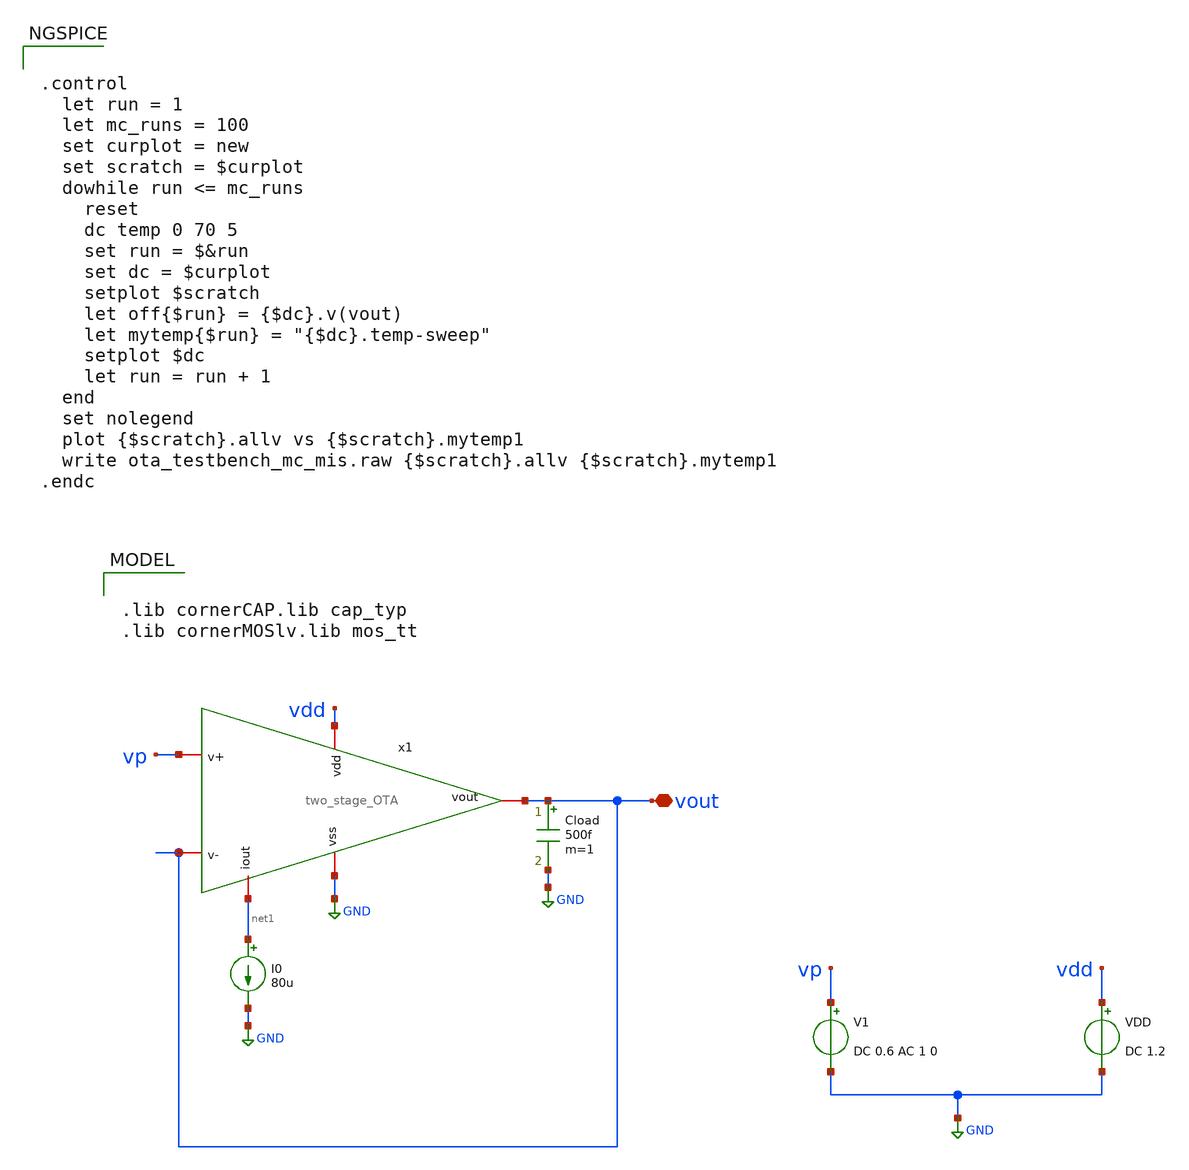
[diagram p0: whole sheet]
** sch_path: modules/module_1_bandgap_reference/part_1_OTA/testbenches/ota_testbench_mc_mis.sch
**.subckt ota_testbench_mc_mis vout
*.iopin vout
V1 vp GND DC 0.6 AC 1 0
VDD vdd GND DC 1.2
I0 net1 GND 80u
Cload vout GND 500f m=1
x1 vdd net1 vp vout vout GND two_stage_OTA
**** begin user architecture code

.lib cornerCAP.lib cap_typ
.lib cornerMOSlv.lib mos_tt



.control
  let run = 1
  let mc_runs = 100
  set curplot = new
  set scratch = $curplot
  dowhile run <= mc_runs
    reset
    dc temp 0 70 5
    set run = $&run
    set dc = $curplot
    setplot $scratch
    let off{$run} = {$dc}.v(vout)
    let mytemp{$run} = "{$dc}.temp-sweep"
    setplot $dc
    let run = run + 1
  end
  set nolegend
  plot {$scratch}.allv vs {$scratch}.mytemp1
  write ota_testbench_mc_mis.raw {$scratch}.allv {$scratch}.mytemp1
.endc



**** end user architecture code
**.ends

* expanding   symbol:  two_stage_OTA.sym # of pins=6
** sym_path: two_stage_OTA.sym
** sch_path: two_stage_OTA.sch
.subckt two_stage_OTA vdd iout v+ v- vout vss
*.iopin v-
*.iopin v+
*.iopin vss
*.iopin vdd
*.iopin iout
*.iopin vout
XM4 vss net1 net3 vss sg13_lv_nmos w=720n l=9.75u ng=1 m=1 mm_ok=1
XM3 vss net1 net1 vss sg13_lv_nmos w=720n l=9.75u ng=1 m=1 mm_ok=1
XM1 net1 v- net2 vdd sg13_lv_pmos w=7.41u l=3.64u ng=1 m=1 mm_ok=1
XM2 net3 v+ net2 vdd sg13_lv_pmos w=7.41u l=3.64u ng=1 m=1 mm_ok=1
XM5 net2 iout vdd vdd sg13_lv_pmos w=5.3u l=1.95u ng=1 m=1 mm_ok=1
XM7 vout iout vdd vdd sg13_lv_pmos w=75u l=2.08u ng=8 m=1 mm_ok=1
XM6 vss net3 vout vss sg13_lv_nmos w=28.8u l=9.75u ng=4 m=1 mm_ok=1
XM9 iout iout vdd vdd sg13_lv_pmos w=75u l=2.08u ng=8 m=1 mm_ok=1
XC2 net3 vout cap_cmim w=22.295e-6 l=22.295e-6 m=1 mm_ok=1
.ends

.GLOBAL GND
.end
